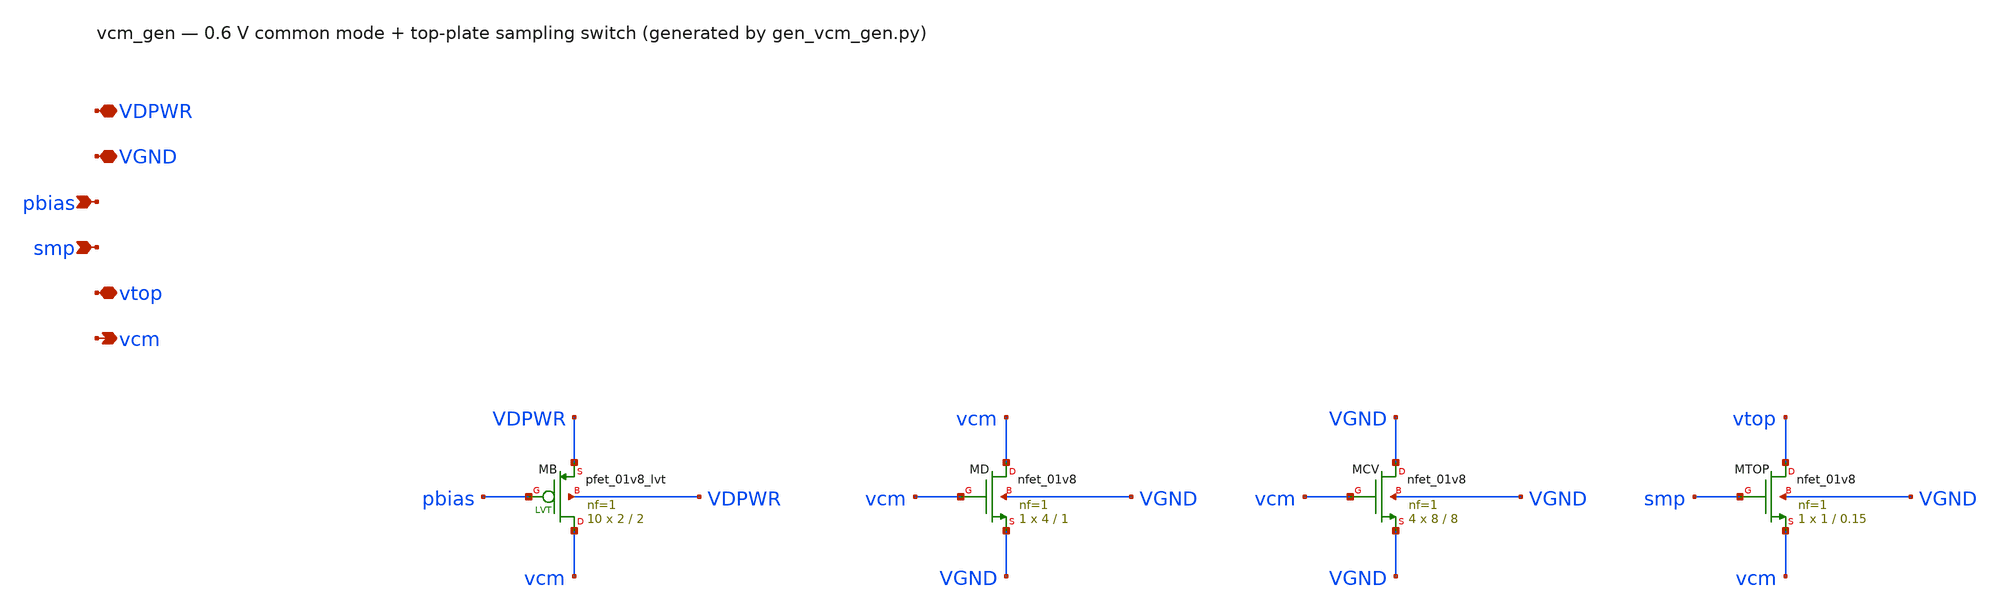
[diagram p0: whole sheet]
** sch_path: xschem/vcm_gen.sch
**.subckt vcm_gen VDPWR VGND pbias smp vtop vcm
*.iopin VDPWR
*.iopin VGND
*.ipin pbias
*.ipin smp
*.iopin vtop
*.opin vcm
XMB vcm pbias VDPWR VDPWR sky130_fd_pr__pfet_01v8_lvt L=2 W=2 nf=1 ad='int((1 + 1)/2) * 2 / 1 * 0.29'
+ as='int((1 + 2)/2) * 2 / 1 * 0.29' pd='2*int((1 + 1)/2) * (2 / 1 + 0.29)' ps='2*int((1 + 2)/2) * (2 / 1 + 0.29)'
+ nrd='0.29 / 2 ' nrs='0.29 / 2 ' sa=0 sb=0 sd=0 mult=10 m=10
XMD vcm vcm VGND VGND sky130_fd_pr__nfet_01v8 L=1 W=4 nf=1 ad='int((1 + 1)/2) * 4 / 1 * 0.29' as='int((1 + 2)/2) * 4 / 1 * 0.29'
+ pd='2*int((1 + 1)/2) * (4 / 1 + 0.29)' ps='2*int((1 + 2)/2) * (4 / 1 + 0.29)' nrd='0.29 / 4 ' nrs='0.29 / 4 '
+ sa=0 sb=0 sd=0 mult=1 m=1
XMCV VGND vcm VGND VGND sky130_fd_pr__nfet_01v8 L=8 W=8 nf=1 ad='int((1 + 1)/2) * 8 / 1 * 0.29' as='int((1 + 2)/2) * 8 / 1 * 0.29'
+ pd='2*int((1 + 1)/2) * (8 / 1 + 0.29)' ps='2*int((1 + 2)/2) * (8 / 1 + 0.29)' nrd='0.29 / 8 ' nrs='0.29 / 8 '
+ sa=0 sb=0 sd=0 mult=4 m=4
XMTOP vtop smp vcm VGND sky130_fd_pr__nfet_01v8 L=0.15 W=1 nf=1 ad='int((1 + 1)/2) * 1 / 1 * 0.29' as='int((1 + 2)/2) * 1 / 1 * 0.29'
+ pd='2*int((1 + 1)/2) * (1 / 1 + 0.29)' ps='2*int((1 + 2)/2) * (1 / 1 + 0.29)' nrd='0.29 / 1 ' nrs='0.29 / 1 '
+ sa=0 sb=0 sd=0 mult=1 m=1
**.ends
.end
